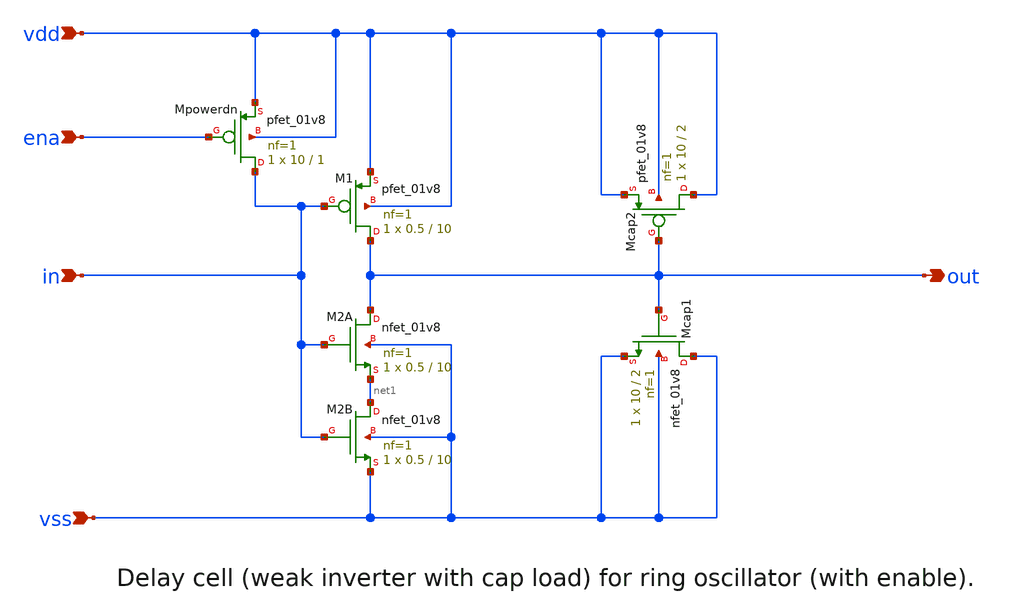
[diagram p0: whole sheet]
** sch_path: xschem/ringosc_delay.sch
**.subckt ringosc_delay vdd vss in out ena
*.ipin vdd
*.ipin vss
*.ipin in
*.opin out
*.ipin ena
XM1 out in vdd vdd sky130_fd_pr__pfet_01v8 L=10 W=0.5 nf=1 ad='int((nf+1)/2) * W/nf * 0.29' as='int((nf+2)/2) * W/nf * 0.29'
+ pd='2*int((nf+1)/2) * (W/nf + 0.29)' ps='2*int((nf+2)/2) * (W/nf + 0.29)' nrd='0.29 / W' nrs='0.29 / W'
+ sa=0 sb=0 sd=0 mult=1 m=1
XM2A out in net1 vss sky130_fd_pr__nfet_01v8 L=10 W=0.5 nf=1 ad='int((nf+1)/2) * W/nf * 0.29' as='int((nf+2)/2) * W/nf * 0.29'
+ pd='2*int((nf+1)/2) * (W/nf + 0.29)' ps='2*int((nf+2)/2) * (W/nf + 0.29)' nrd='0.29 / W' nrs='0.29 / W'
+ sa=0 sb=0 sd=0 mult=1 m=1
XMcap1 vss out vss vss sky130_fd_pr__nfet_01v8 L=2 W=10 nf=1 ad='int((nf+1)/2) * W/nf * 0.29' as='int((nf+2)/2) * W/nf * 0.29'
+ pd='2*int((nf+1)/2) * (W/nf + 0.29)' ps='2*int((nf+2)/2) * (W/nf + 0.29)' nrd='0.29 / W' nrs='0.29 / W'
+ sa=0 sb=0 sd=0 mult=1 m=1
XMcap2 vdd out vdd vdd sky130_fd_pr__pfet_01v8 L=2 W=10 nf=1 ad='int((nf+1)/2) * W/nf * 0.29' as='int((nf+2)/2) * W/nf * 0.29'
+ pd='2*int((nf+1)/2) * (W/nf + 0.29)' ps='2*int((nf+2)/2) * (W/nf + 0.29)' nrd='0.29 / W' nrs='0.29 / W'
+ sa=0 sb=0 sd=0 mult=1 m=1
XM2B net1 in vss vss sky130_fd_pr__nfet_01v8 L=10 W=0.5 nf=1 ad='int((nf+1)/2) * W/nf * 0.29' as='int((nf+2)/2) * W/nf * 0.29'
+ pd='2*int((nf+1)/2) * (W/nf + 0.29)' ps='2*int((nf+2)/2) * (W/nf + 0.29)' nrd='0.29 / W' nrs='0.29 / W'
+ sa=0 sb=0 sd=0 mult=1 m=1
XMpowerdn in ena vdd vdd sky130_fd_pr__pfet_01v8 L=1 W=10 nf=1 ad='int((nf+1)/2) * W/nf * 0.29' as='int((nf+2)/2) * W/nf * 0.29'
+ pd='2*int((nf+1)/2) * (W/nf + 0.29)' ps='2*int((nf+2)/2) * (W/nf + 0.29)' nrd='0.29 / W' nrs='0.29 / W'
+ sa=0 sb=0 sd=0 mult=1 m=1
**.ends
.end
